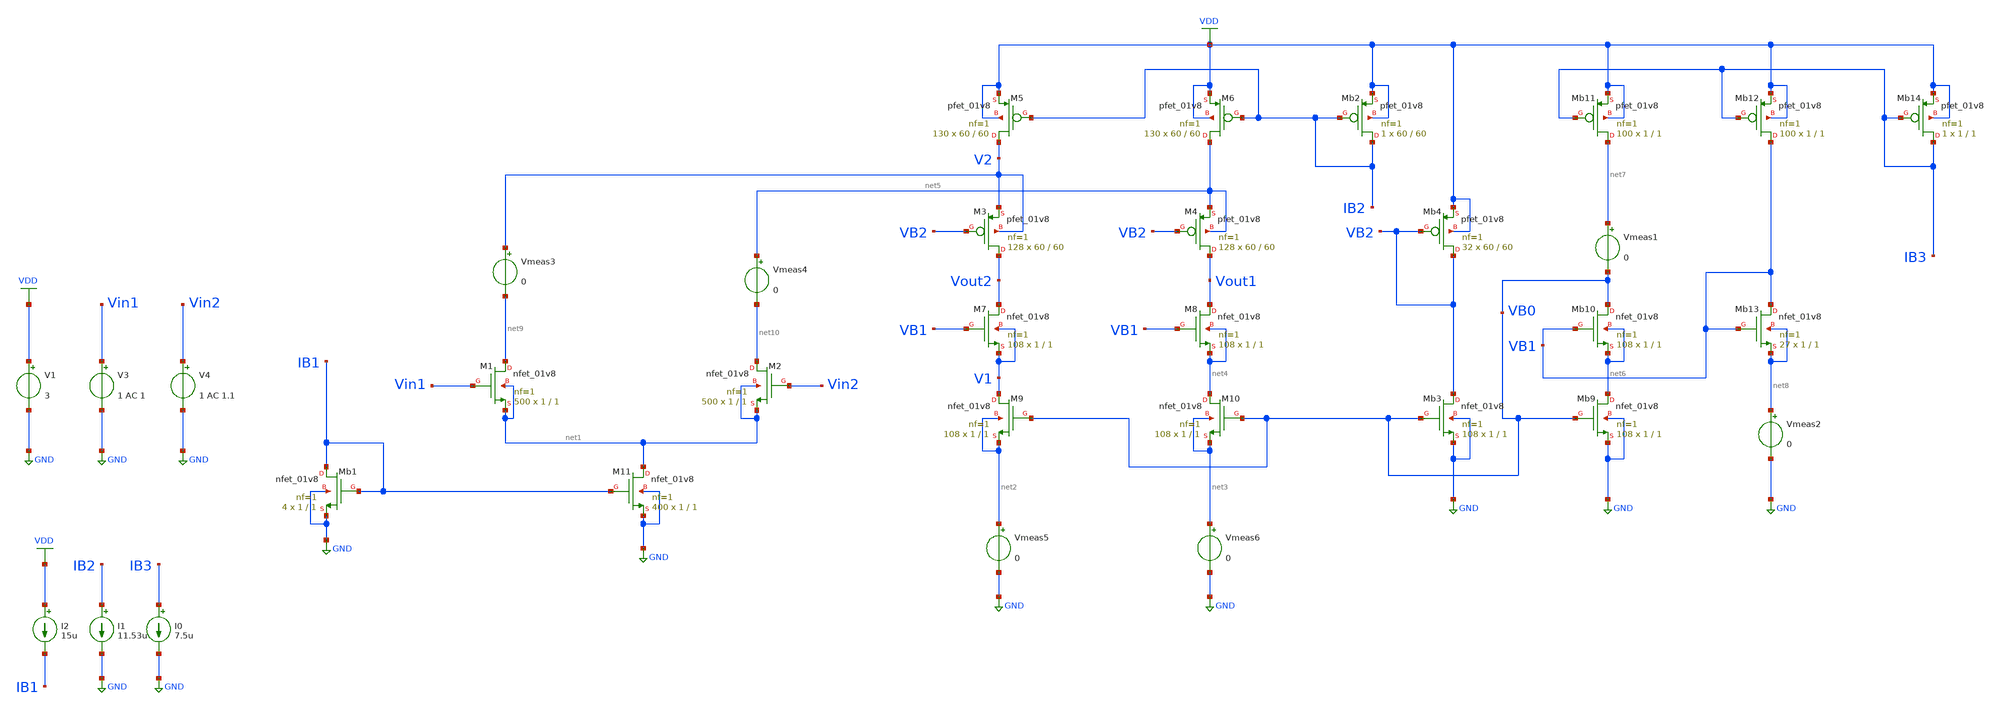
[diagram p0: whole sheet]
** sch_path: Circuits/Examples/Analog/Folded_Cascode/Folded_Cascode.sch
**.subckt Folded_Cascode
V1 VDD GND 3
XM11 net1 IB1 GND GND sky130_fd_pr__nfet_01v8 L=1 W=1 nf=1 ad='int((nf+1)/2) * W/nf * 0.29' as='int((nf+2)/2) * W/nf * 0.29'
+ pd='2*int((nf+1)/2) * (W/nf + 0.29)' ps='2*int((nf+2)/2) * (W/nf + 0.29)' nrd='0.29 / W' nrs='0.29 / W'
+ sa=0 sb=0 sd=0 mult=400 m=400
XM1 net9 Vin1 net1 net1 sky130_fd_pr__nfet_01v8 L=1 W=1 nf=1 ad='int((nf+1)/2) * W/nf * 0.29' as='int((nf+2)/2) * W/nf * 0.29'
+ pd='2*int((nf+1)/2) * (W/nf + 0.29)' ps='2*int((nf+2)/2) * (W/nf + 0.29)' nrd='0.29 / W' nrs='0.29 / W'
+ sa=0 sb=0 sd=0 mult=500 m=500
XM2 net10 Vin2 net1 net1 sky130_fd_pr__nfet_01v8 L=1 W=1 nf=1 ad='int((nf+1)/2) * W/nf * 0.29' as='int((nf+2)/2) * W/nf * 0.29'
+ pd='2*int((nf+1)/2) * (W/nf + 0.29)' ps='2*int((nf+2)/2) * (W/nf + 0.29)' nrd='0.29 / W' nrs='0.29 / W'
+ sa=0 sb=0 sd=0 mult=500 m=500
XM9 V1 VB0 net2 net2 sky130_fd_pr__nfet_01v8 L=1 W=1 nf=1 ad='int((nf+1)/2) * W/nf * 0.29' as='int((nf+2)/2) * W/nf * 0.29'
+ pd='2*int((nf+1)/2) * (W/nf + 0.29)' ps='2*int((nf+2)/2) * (W/nf + 0.29)' nrd='0.29 / W' nrs='0.29 / W'
+ sa=0 sb=0 sd=0 mult=108 m=108
XM10 net4 VB0 net3 net3 sky130_fd_pr__nfet_01v8 L=1 W=1 nf=1 ad='int((nf+1)/2) * W/nf * 0.29' as='int((nf+2)/2) * W/nf * 0.29'
+ pd='2*int((nf+1)/2) * (W/nf + 0.29)' ps='2*int((nf+2)/2) * (W/nf + 0.29)' nrd='0.29 / W' nrs='0.29 / W'
+ sa=0 sb=0 sd=0 mult=108 m=108
XM7 Vout2 VB1 V1 V1 sky130_fd_pr__nfet_01v8 L=1 W=1 nf=1 ad='int((nf+1)/2) * W/nf * 0.29' as='int((nf+2)/2) * W/nf * 0.29'
+ pd='2*int((nf+1)/2) * (W/nf + 0.29)' ps='2*int((nf+2)/2) * (W/nf + 0.29)' nrd='0.29 / W' nrs='0.29 / W'
+ sa=0 sb=0 sd=0 mult=108 m=108
XM8 Vout1 VB1 net4 net4 sky130_fd_pr__nfet_01v8 L=1 W=1 nf=1 ad='int((nf+1)/2) * W/nf * 0.29' as='int((nf+2)/2) * W/nf * 0.29'
+ pd='2*int((nf+1)/2) * (W/nf + 0.29)' ps='2*int((nf+2)/2) * (W/nf + 0.29)' nrd='0.29 / W' nrs='0.29 / W'
+ sa=0 sb=0 sd=0 mult=108 m=108
XM3 Vout2 VB2 V2 V2 sky130_fd_pr__pfet_01v8 L=60 W=60 nf=1 ad='int((nf+1)/2) * W/nf * 0.29' as='int((nf+2)/2) * W/nf * 0.29'
+ pd='2*int((nf+1)/2) * (W/nf + 0.29)' ps='2*int((nf+2)/2) * (W/nf + 0.29)' nrd='0.29 / W' nrs='0.29 / W'
+ sa=0 sb=0 sd=0 mult=128 m=128
XM4 Vout1 VB2 net5 net5 sky130_fd_pr__pfet_01v8 L=60 W=60 nf=1 ad='int((nf+1)/2) * W/nf * 0.29' as='int((nf+2)/2) * W/nf * 0.29'
+ pd='2*int((nf+1)/2) * (W/nf + 0.29)' ps='2*int((nf+2)/2) * (W/nf + 0.29)' nrd='0.29 / W' nrs='0.29 / W'
+ sa=0 sb=0 sd=0 mult=128 m=128
XM5 V2 IB2 VDD VDD sky130_fd_pr__pfet_01v8 L=60 W=60 nf=1 ad='int((nf+1)/2) * W/nf * 0.29' as='int((nf+2)/2) * W/nf * 0.29'
+ pd='2*int((nf+1)/2) * (W/nf + 0.29)' ps='2*int((nf+2)/2) * (W/nf + 0.29)' nrd='0.29 / W' nrs='0.29 / W'
+ sa=0 sb=0 sd=0 mult=130 m=130
XM6 net5 IB2 VDD VDD sky130_fd_pr__pfet_01v8 L=60 W=60 nf=1 ad='int((nf+1)/2) * W/nf * 0.29' as='int((nf+2)/2) * W/nf * 0.29'
+ pd='2*int((nf+1)/2) * (W/nf + 0.29)' ps='2*int((nf+2)/2) * (W/nf + 0.29)' nrd='0.29 / W' nrs='0.29 / W'
+ sa=0 sb=0 sd=0 mult=130 m=130
XMb2 IB2 IB2 VDD VDD sky130_fd_pr__pfet_01v8 L=60 W=60 nf=1 ad='int((nf+1)/2) * W/nf * 0.29' as='int((nf+2)/2) * W/nf * 0.29'
+ pd='2*int((nf+1)/2) * (W/nf + 0.29)' ps='2*int((nf+2)/2) * (W/nf + 0.29)' nrd='0.29 / W' nrs='0.29 / W'
+ sa=0 sb=0 sd=0 mult=1 m=1
XMb1 IB1 IB1 GND GND sky130_fd_pr__nfet_01v8 L=1 W=1 nf=1 ad='int((nf+1)/2) * W/nf * 0.29' as='int((nf+2)/2) * W/nf * 0.29'
+ pd='2*int((nf+1)/2) * (W/nf + 0.29)' ps='2*int((nf+2)/2) * (W/nf + 0.29)' nrd='0.29 / W' nrs='0.29 / W'
+ sa=0 sb=0 sd=0 mult=4 m=4
I0 IB3 GND 7.5u
I1 IB2 GND 11.53u
I2 VDD IB1 15u
V3 Vin1 GND 1 AC 1
V4 Vin2 GND 1 AC 1.1
XMb9 net6 VB0 GND GND sky130_fd_pr__nfet_01v8 L=1 W=1 nf=1 ad='int((nf+1)/2) * W/nf * 0.29' as='int((nf+2)/2) * W/nf * 0.29'
+ pd='2*int((nf+1)/2) * (W/nf + 0.29)' ps='2*int((nf+2)/2) * (W/nf + 0.29)' nrd='0.29 / W' nrs='0.29 / W'
+ sa=0 sb=0 sd=0 mult=108 m=108
XMb10 VB0 VB1 net6 net6 sky130_fd_pr__nfet_01v8 L=1 W=1 nf=1 ad='int((nf+1)/2) * W/nf * 0.29' as='int((nf+2)/2) * W/nf * 0.29'
+ pd='2*int((nf+1)/2) * (W/nf + 0.29)' ps='2*int((nf+2)/2) * (W/nf + 0.29)' nrd='0.29 / W' nrs='0.29 / W'
+ sa=0 sb=0 sd=0 mult=108 m=108
XMb11 net7 IB3 VDD VDD sky130_fd_pr__pfet_01v8 L=1 W=1 nf=1 ad='int((nf+1)/2) * W/nf * 0.29' as='int((nf+2)/2) * W/nf * 0.29'
+ pd='2*int((nf+1)/2) * (W/nf + 0.29)' ps='2*int((nf+2)/2) * (W/nf + 0.29)' nrd='0.29 / W' nrs='0.29 / W'
+ sa=0 sb=0 sd=0 mult=100 m=100
XMb12 VB1 IB3 VDD VDD sky130_fd_pr__pfet_01v8 L=1 W=1 nf=1 ad='int((nf+1)/2) * W/nf * 0.29' as='int((nf+2)/2) * W/nf * 0.29'
+ pd='2*int((nf+1)/2) * (W/nf + 0.29)' ps='2*int((nf+2)/2) * (W/nf + 0.29)' nrd='0.29 / W' nrs='0.29 / W'
+ sa=0 sb=0 sd=0 mult=100 m=100
XMb13 VB1 VB1 net8 net8 sky130_fd_pr__nfet_01v8 L=1 W=1 nf=1 ad='int((nf+1)/2) * W/nf * 0.29' as='int((nf+2)/2) * W/nf * 0.29'
+ pd='2*int((nf+1)/2) * (W/nf + 0.29)' ps='2*int((nf+2)/2) * (W/nf + 0.29)' nrd='0.29 / W' nrs='0.29 / W'
+ sa=0 sb=0 sd=0 mult=27 m=27
XMb14 IB3 IB3 VDD VDD sky130_fd_pr__pfet_01v8 L=1 W=1 nf=1 ad='int((nf+1)/2) * W/nf * 0.29' as='int((nf+2)/2) * W/nf * 0.29'
+ pd='2*int((nf+1)/2) * (W/nf + 0.29)' ps='2*int((nf+2)/2) * (W/nf + 0.29)' nrd='0.29 / W' nrs='0.29 / W'
+ sa=0 sb=0 sd=0 mult=1 m=1
Vmeas1 net7 VB0 0
Vmeas2 net8 GND 0
XMb3 VB2 VB0 GND GND sky130_fd_pr__nfet_01v8 L=1 W=1 nf=1 ad='int((nf+1)/2) * W/nf * 0.29' as='int((nf+2)/2) * W/nf * 0.29'
+ pd='2*int((nf+1)/2) * (W/nf + 0.29)' ps='2*int((nf+2)/2) * (W/nf + 0.29)' nrd='0.29 / W' nrs='0.29 / W'
+ sa=0 sb=0 sd=0 mult=108 m=108
XMb4 VB2 VB2 VDD VDD sky130_fd_pr__pfet_01v8 L=60 W=60 nf=1 ad='int((nf+1)/2) * W/nf * 0.29' as='int((nf+2)/2) * W/nf * 0.29'
+ pd='2*int((nf+1)/2) * (W/nf + 0.29)' ps='2*int((nf+2)/2) * (W/nf + 0.29)' nrd='0.29 / W' nrs='0.29 / W'
+ sa=0 sb=0 sd=0 mult=32 m=32
Vmeas3 V2 net9 0
Vmeas4 net5 net10 0
Vmeas5 net2 GND 0
Vmeas6 net3 GND 0
**** begin user architecture code
 ** manual skywater pdks install (with patches applied)
* .lib $::SKYWATER_MODELS/models/sky130.lib.spice tt

** opencircuitdesign pdks install
.lib $::SKYWATER_MODELS/sky130.lib.spice tt

.param mc_mm_switch=0
.param mc_pr_switch=0



*.tran 10u 1
.ac dec 20 1 1e12
.control
run
plot db(Vout2-Vout1)
*plot v(V1)
*plot (v(Vout2)-v(V1))
*plot (v(V2)-v(Vout2))
*plot i(Vmeas5)
*plot v(Vout2)
.endc
.save all

**** end user architecture code
**.ends
.GLOBAL GND
.GLOBAL VDD
.end
